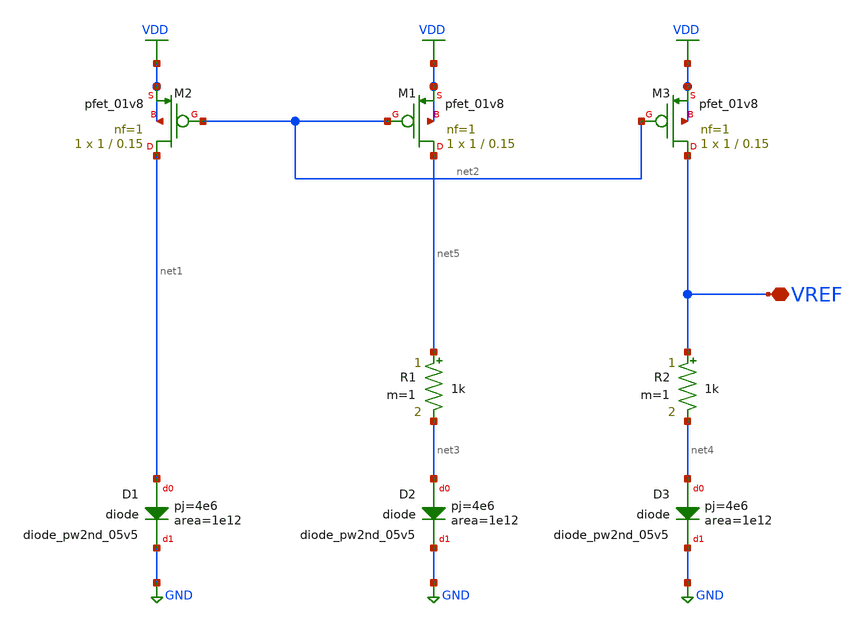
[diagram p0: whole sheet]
** sch_path: design/CNR_GR02_SKY130NM/CNR_GR02.sch
**.subckt CNR_GR02 VREF
*.iopin VREF
XM2 net1 net2 VDD VDD sky130_fd_pr__pfet_01v8 L=0.15 W=1 nf=1 ad='int((nf+1)/2) * W/nf * 0.29' as='int((nf+2)/2) * W/nf * 0.29'
+ pd='2*int((nf+1)/2) * (W/nf + 0.29)' ps='2*int((nf+2)/2) * (W/nf + 0.29)' nrd='0.29 / W' nrs='0.29 / W'
+ sa=0 sb=0 sd=0 mult=1 m=1
XM1 net5 net2 VDD VDD sky130_fd_pr__pfet_01v8 L=0.15 W=1 nf=1 ad='int((nf+1)/2) * W/nf * 0.29' as='int((nf+2)/2) * W/nf * 0.29'
+ pd='2*int((nf+1)/2) * (W/nf + 0.29)' ps='2*int((nf+2)/2) * (W/nf + 0.29)' nrd='0.29 / W' nrs='0.29 / W'
+ sa=0 sb=0 sd=0 mult=1 m=1
XM3 VREF net2 VDD VDD sky130_fd_pr__pfet_01v8 L=0.15 W=1 nf=1 ad='int((nf+1)/2) * W/nf * 0.29' as='int((nf+2)/2) * W/nf * 0.29'
+ pd='2*int((nf+1)/2) * (W/nf + 0.29)' ps='2*int((nf+2)/2) * (W/nf + 0.29)' nrd='0.29 / W' nrs='0.29 / W'
+ sa=0 sb=0 sd=0 mult=1 m=1
XD1 net1 GND sky130_fd_pr__diode_pw2nd_05v5 area=1e12 pj=4e6
XD2 net3 GND sky130_fd_pr__diode_pw2nd_05v5 area=1e12 pj=4e6
XD3 net4 GND sky130_fd_pr__diode_pw2nd_05v5 area=1e12 pj=4e6
R1 net5 net3 1k m=1
R2 VREF net4 1k m=1
**.ends
.GLOBAL GND
.GLOBAL VDD
.end
